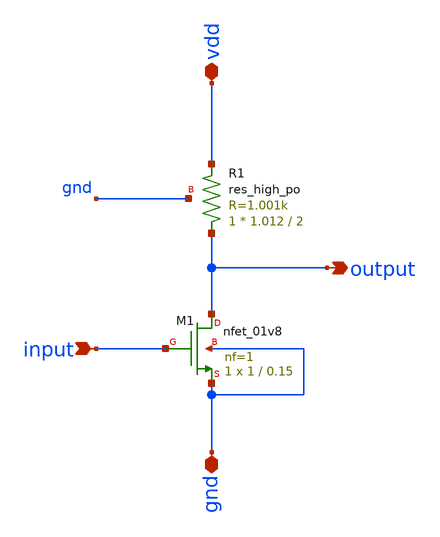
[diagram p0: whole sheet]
** sch_path: xschem/1.sch
**.subckt 1 input vdd gnd output
*.ipin input
*.iopin vdd
*.iopin gnd
*.opin output
XM1 output input gnd gnd sky130_fd_pr__nfet_01v8 L=0.15 W=1 nf=1 ad='int((nf+1)/2) * W/nf * 0.29' as='int((nf+2)/2) * W/nf * 0.29'
+ pd='2*int((nf+1)/2) * (W/nf + 0.29)' ps='2*int((nf+2)/2) * (W/nf + 0.29)' nrd='0.29 / W' nrs='0.29 / W'
+ sa=0 sb=0 sd=0 mult=1 m=1
XR1 output vdd gnd sky130_fd_pr__res_high_po W=1.012 L=2 mult=1 m=1
**.ends
.end
